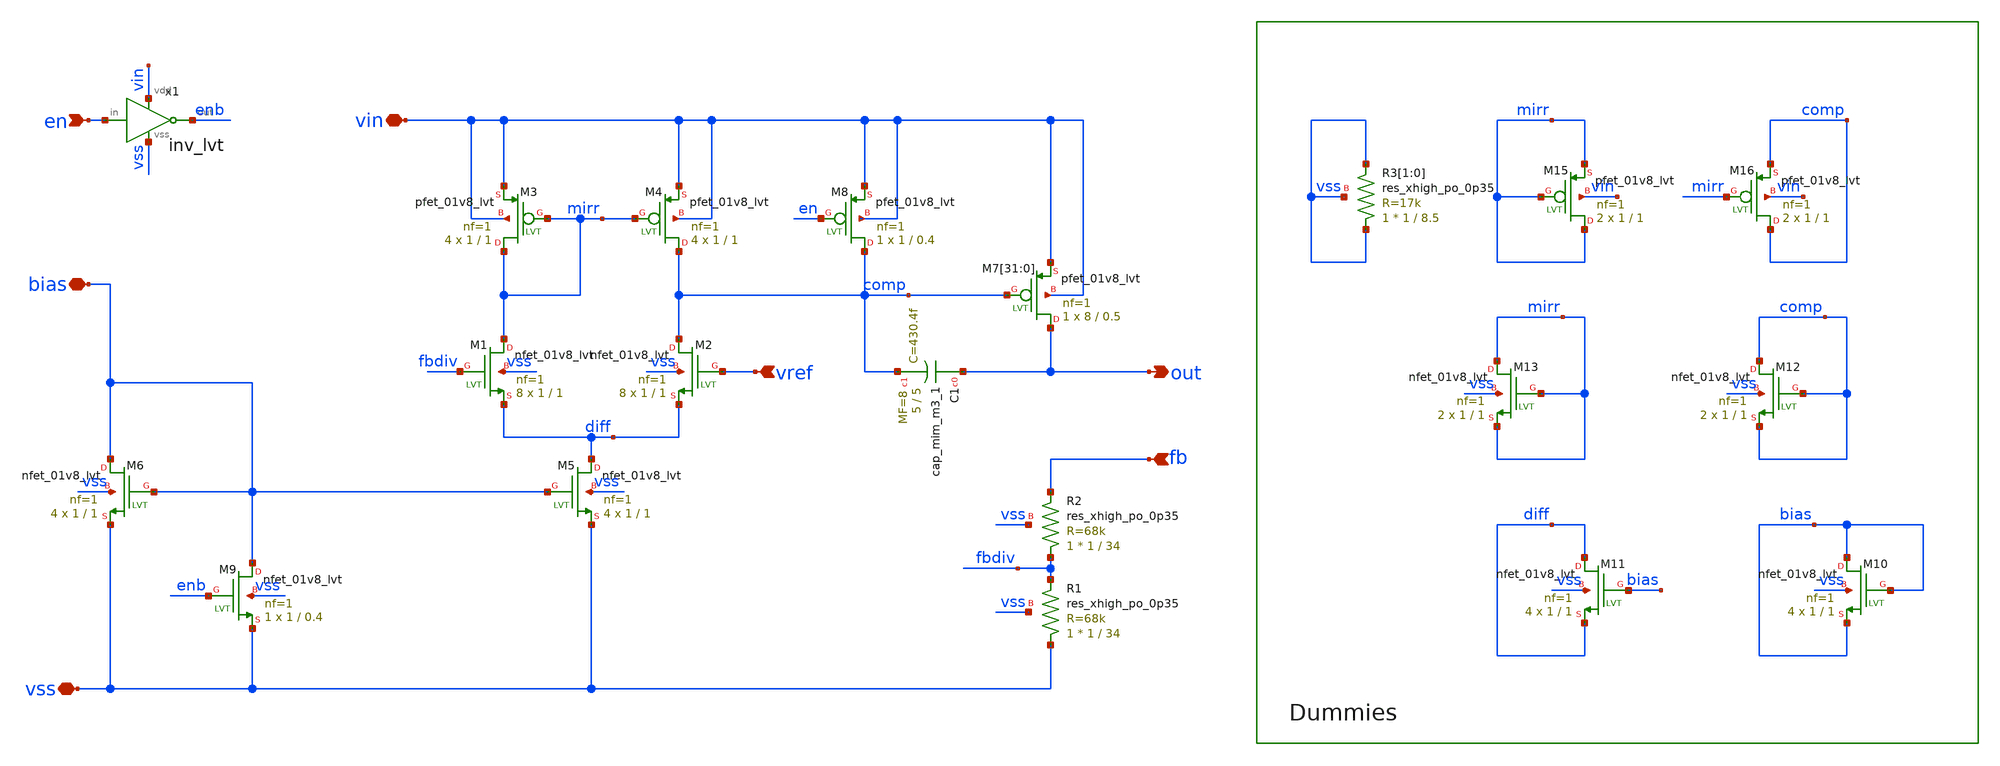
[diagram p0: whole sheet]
** sch_path: xschem/regulator/regulator.sch
**.subckt regulator vin vss vref out bias en fb
*.iopin vin
*.iopin vss
*.ipin vref
*.opin out
*.iopin bias
*.ipin en
*.ipin fb
XM2 comp vref diff vss sky130_fd_pr__nfet_01v8_lvt L=1 W=1 nf=1 ad='int((nf+1)/2) * W/nf * 0.29' as='int((nf+2)/2) * W/nf * 0.29'
+ pd='2*int((nf+1)/2) * (W/nf + 0.29)' ps='2*int((nf+2)/2) * (W/nf + 0.29)' nrd='0.29 / W' nrs='0.29 / W'
+ sa=0 sb=0 sd=0 mult=8 m=8
XM1 mirr fbdiv diff vss sky130_fd_pr__nfet_01v8_lvt L=1 W=1 nf=1 ad='int((nf+1)/2) * W/nf * 0.29' as='int((nf+2)/2) * W/nf * 0.29'
+ pd='2*int((nf+1)/2) * (W/nf + 0.29)' ps='2*int((nf+2)/2) * (W/nf + 0.29)' nrd='0.29 / W' nrs='0.29 / W'
+ sa=0 sb=0 sd=0 mult=8 m=8
XM5 diff bias vss vss sky130_fd_pr__nfet_01v8_lvt L=1 W=1 nf=1 ad='int((nf+1)/2) * W/nf * 0.29' as='int((nf+2)/2) * W/nf * 0.29'
+ pd='2*int((nf+1)/2) * (W/nf + 0.29)' ps='2*int((nf+2)/2) * (W/nf + 0.29)' nrd='0.29 / W' nrs='0.29 / W'
+ sa=0 sb=0 sd=0 mult=4 m=4
XM4 comp mirr vin vin sky130_fd_pr__pfet_01v8_lvt L=1 W=1 nf=1 ad='int((nf+1)/2) * W/nf * 0.29' as='int((nf+2)/2) * W/nf * 0.29'
+ pd='2*int((nf+1)/2) * (W/nf + 0.29)' ps='2*int((nf+2)/2) * (W/nf + 0.29)' nrd='0.29 / W' nrs='0.29 / W'
+ sa=0 sb=0 sd=0 mult=4 m=4
XM3 mirr mirr vin vin sky130_fd_pr__pfet_01v8_lvt L=1 W=1 nf=1 ad='int((nf+1)/2) * W/nf * 0.29' as='int((nf+2)/2) * W/nf * 0.29'
+ pd='2*int((nf+1)/2) * (W/nf + 0.29)' ps='2*int((nf+2)/2) * (W/nf + 0.29)' nrd='0.29 / W' nrs='0.29 / W'
+ sa=0 sb=0 sd=0 mult=4 m=4
XM6 bias bias vss vss sky130_fd_pr__nfet_01v8_lvt L=1 W=1 nf=1 ad='int((nf+1)/2) * W/nf * 0.29' as='int((nf+2)/2) * W/nf * 0.29'
+ pd='2*int((nf+1)/2) * (W/nf + 0.29)' ps='2*int((nf+2)/2) * (W/nf + 0.29)' nrd='0.29 / W' nrs='0.29 / W'
+ sa=0 sb=0 sd=0 mult=4 m=4
XM7[31] out comp vin vin sky130_fd_pr__pfet_01v8_lvt L=0.5 W=8 nf=1 ad='int((nf+1)/2) * W/nf * 0.29'
+ as='int((nf+2)/2) * W/nf * 0.29' pd='2*int((nf+1)/2) * (W/nf + 0.29)' ps='2*int((nf+2)/2) * (W/nf + 0.29)'
+ nrd='0.29 / W' nrs='0.29 / W' sa=0 sb=0 sd=0 mult=1 m=1
XM7[30] out comp vin vin sky130_fd_pr__pfet_01v8_lvt L=0.5 W=8 nf=1 ad='int((nf+1)/2) * W/nf * 0.29'
+ as='int((nf+2)/2) * W/nf * 0.29' pd='2*int((nf+1)/2) * (W/nf + 0.29)' ps='2*int((nf+2)/2) * (W/nf + 0.29)'
+ nrd='0.29 / W' nrs='0.29 / W' sa=0 sb=0 sd=0 mult=1 m=1
XM7[29] out comp vin vin sky130_fd_pr__pfet_01v8_lvt L=0.5 W=8 nf=1 ad='int((nf+1)/2) * W/nf * 0.29'
+ as='int((nf+2)/2) * W/nf * 0.29' pd='2*int((nf+1)/2) * (W/nf + 0.29)' ps='2*int((nf+2)/2) * (W/nf + 0.29)'
+ nrd='0.29 / W' nrs='0.29 / W' sa=0 sb=0 sd=0 mult=1 m=1
XM7[28] out comp vin vin sky130_fd_pr__pfet_01v8_lvt L=0.5 W=8 nf=1 ad='int((nf+1)/2) * W/nf * 0.29'
+ as='int((nf+2)/2) * W/nf * 0.29' pd='2*int((nf+1)/2) * (W/nf + 0.29)' ps='2*int((nf+2)/2) * (W/nf + 0.29)'
+ nrd='0.29 / W' nrs='0.29 / W' sa=0 sb=0 sd=0 mult=1 m=1
XM7[27] out comp vin vin sky130_fd_pr__pfet_01v8_lvt L=0.5 W=8 nf=1 ad='int((nf+1)/2) * W/nf * 0.29'
+ as='int((nf+2)/2) * W/nf * 0.29' pd='2*int((nf+1)/2) * (W/nf + 0.29)' ps='2*int((nf+2)/2) * (W/nf + 0.29)'
+ nrd='0.29 / W' nrs='0.29 / W' sa=0 sb=0 sd=0 mult=1 m=1
XM7[26] out comp vin vin sky130_fd_pr__pfet_01v8_lvt L=0.5 W=8 nf=1 ad='int((nf+1)/2) * W/nf * 0.29'
+ as='int((nf+2)/2) * W/nf * 0.29' pd='2*int((nf+1)/2) * (W/nf + 0.29)' ps='2*int((nf+2)/2) * (W/nf + 0.29)'
+ nrd='0.29 / W' nrs='0.29 / W' sa=0 sb=0 sd=0 mult=1 m=1
XM7[25] out comp vin vin sky130_fd_pr__pfet_01v8_lvt L=0.5 W=8 nf=1 ad='int((nf+1)/2) * W/nf * 0.29'
+ as='int((nf+2)/2) * W/nf * 0.29' pd='2*int((nf+1)/2) * (W/nf + 0.29)' ps='2*int((nf+2)/2) * (W/nf + 0.29)'
+ nrd='0.29 / W' nrs='0.29 / W' sa=0 sb=0 sd=0 mult=1 m=1
XM7[24] out comp vin vin sky130_fd_pr__pfet_01v8_lvt L=0.5 W=8 nf=1 ad='int((nf+1)/2) * W/nf * 0.29'
+ as='int((nf+2)/2) * W/nf * 0.29' pd='2*int((nf+1)/2) * (W/nf + 0.29)' ps='2*int((nf+2)/2) * (W/nf + 0.29)'
+ nrd='0.29 / W' nrs='0.29 / W' sa=0 sb=0 sd=0 mult=1 m=1
XM7[23] out comp vin vin sky130_fd_pr__pfet_01v8_lvt L=0.5 W=8 nf=1 ad='int((nf+1)/2) * W/nf * 0.29'
+ as='int((nf+2)/2) * W/nf * 0.29' pd='2*int((nf+1)/2) * (W/nf + 0.29)' ps='2*int((nf+2)/2) * (W/nf + 0.29)'
+ nrd='0.29 / W' nrs='0.29 / W' sa=0 sb=0 sd=0 mult=1 m=1
XM7[22] out comp vin vin sky130_fd_pr__pfet_01v8_lvt L=0.5 W=8 nf=1 ad='int((nf+1)/2) * W/nf * 0.29'
+ as='int((nf+2)/2) * W/nf * 0.29' pd='2*int((nf+1)/2) * (W/nf + 0.29)' ps='2*int((nf+2)/2) * (W/nf + 0.29)'
+ nrd='0.29 / W' nrs='0.29 / W' sa=0 sb=0 sd=0 mult=1 m=1
XM7[21] out comp vin vin sky130_fd_pr__pfet_01v8_lvt L=0.5 W=8 nf=1 ad='int((nf+1)/2) * W/nf * 0.29'
+ as='int((nf+2)/2) * W/nf * 0.29' pd='2*int((nf+1)/2) * (W/nf + 0.29)' ps='2*int((nf+2)/2) * (W/nf + 0.29)'
+ nrd='0.29 / W' nrs='0.29 / W' sa=0 sb=0 sd=0 mult=1 m=1
XM7[20] out comp vin vin sky130_fd_pr__pfet_01v8_lvt L=0.5 W=8 nf=1 ad='int((nf+1)/2) * W/nf * 0.29'
+ as='int((nf+2)/2) * W/nf * 0.29' pd='2*int((nf+1)/2) * (W/nf + 0.29)' ps='2*int((nf+2)/2) * (W/nf + 0.29)'
+ nrd='0.29 / W' nrs='0.29 / W' sa=0 sb=0 sd=0 mult=1 m=1
XM7[19] out comp vin vin sky130_fd_pr__pfet_01v8_lvt L=0.5 W=8 nf=1 ad='int((nf+1)/2) * W/nf * 0.29'
+ as='int((nf+2)/2) * W/nf * 0.29' pd='2*int((nf+1)/2) * (W/nf + 0.29)' ps='2*int((nf+2)/2) * (W/nf + 0.29)'
+ nrd='0.29 / W' nrs='0.29 / W' sa=0 sb=0 sd=0 mult=1 m=1
XM7[18] out comp vin vin sky130_fd_pr__pfet_01v8_lvt L=0.5 W=8 nf=1 ad='int((nf+1)/2) * W/nf * 0.29'
+ as='int((nf+2)/2) * W/nf * 0.29' pd='2*int((nf+1)/2) * (W/nf + 0.29)' ps='2*int((nf+2)/2) * (W/nf + 0.29)'
+ nrd='0.29 / W' nrs='0.29 / W' sa=0 sb=0 sd=0 mult=1 m=1
XM7[17] out comp vin vin sky130_fd_pr__pfet_01v8_lvt L=0.5 W=8 nf=1 ad='int((nf+1)/2) * W/nf * 0.29'
+ as='int((nf+2)/2) * W/nf * 0.29' pd='2*int((nf+1)/2) * (W/nf + 0.29)' ps='2*int((nf+2)/2) * (W/nf + 0.29)'
+ nrd='0.29 / W' nrs='0.29 / W' sa=0 sb=0 sd=0 mult=1 m=1
XM7[16] out comp vin vin sky130_fd_pr__pfet_01v8_lvt L=0.5 W=8 nf=1 ad='int((nf+1)/2) * W/nf * 0.29'
+ as='int((nf+2)/2) * W/nf * 0.29' pd='2*int((nf+1)/2) * (W/nf + 0.29)' ps='2*int((nf+2)/2) * (W/nf + 0.29)'
+ nrd='0.29 / W' nrs='0.29 / W' sa=0 sb=0 sd=0 mult=1 m=1
XM7[15] out comp vin vin sky130_fd_pr__pfet_01v8_lvt L=0.5 W=8 nf=1 ad='int((nf+1)/2) * W/nf * 0.29'
+ as='int((nf+2)/2) * W/nf * 0.29' pd='2*int((nf+1)/2) * (W/nf + 0.29)' ps='2*int((nf+2)/2) * (W/nf + 0.29)'
+ nrd='0.29 / W' nrs='0.29 / W' sa=0 sb=0 sd=0 mult=1 m=1
XM7[14] out comp vin vin sky130_fd_pr__pfet_01v8_lvt L=0.5 W=8 nf=1 ad='int((nf+1)/2) * W/nf * 0.29'
+ as='int((nf+2)/2) * W/nf * 0.29' pd='2*int((nf+1)/2) * (W/nf + 0.29)' ps='2*int((nf+2)/2) * (W/nf + 0.29)'
+ nrd='0.29 / W' nrs='0.29 / W' sa=0 sb=0 sd=0 mult=1 m=1
XM7[13] out comp vin vin sky130_fd_pr__pfet_01v8_lvt L=0.5 W=8 nf=1 ad='int((nf+1)/2) * W/nf * 0.29'
+ as='int((nf+2)/2) * W/nf * 0.29' pd='2*int((nf+1)/2) * (W/nf + 0.29)' ps='2*int((nf+2)/2) * (W/nf + 0.29)'
+ nrd='0.29 / W' nrs='0.29 / W' sa=0 sb=0 sd=0 mult=1 m=1
XM7[12] out comp vin vin sky130_fd_pr__pfet_01v8_lvt L=0.5 W=8 nf=1 ad='int((nf+1)/2) * W/nf * 0.29'
+ as='int((nf+2)/2) * W/nf * 0.29' pd='2*int((nf+1)/2) * (W/nf + 0.29)' ps='2*int((nf+2)/2) * (W/nf + 0.29)'
+ nrd='0.29 / W' nrs='0.29 / W' sa=0 sb=0 sd=0 mult=1 m=1
XM7[11] out comp vin vin sky130_fd_pr__pfet_01v8_lvt L=0.5 W=8 nf=1 ad='int((nf+1)/2) * W/nf * 0.29'
+ as='int((nf+2)/2) * W/nf * 0.29' pd='2*int((nf+1)/2) * (W/nf + 0.29)' ps='2*int((nf+2)/2) * (W/nf + 0.29)'
+ nrd='0.29 / W' nrs='0.29 / W' sa=0 sb=0 sd=0 mult=1 m=1
XM7[10] out comp vin vin sky130_fd_pr__pfet_01v8_lvt L=0.5 W=8 nf=1 ad='int((nf+1)/2) * W/nf * 0.29'
+ as='int((nf+2)/2) * W/nf * 0.29' pd='2*int((nf+1)/2) * (W/nf + 0.29)' ps='2*int((nf+2)/2) * (W/nf + 0.29)'
+ nrd='0.29 / W' nrs='0.29 / W' sa=0 sb=0 sd=0 mult=1 m=1
XM7[9] out comp vin vin sky130_fd_pr__pfet_01v8_lvt L=0.5 W=8 nf=1 ad='int((nf+1)/2) * W/nf * 0.29' as='int((nf+2)/2) * W/nf * 0.29'
+ pd='2*int((nf+1)/2) * (W/nf + 0.29)' ps='2*int((nf+2)/2) * (W/nf + 0.29)' nrd='0.29 / W' nrs='0.29 / W'
+ sa=0 sb=0 sd=0 mult=1 m=1
XM7[8] out comp vin vin sky130_fd_pr__pfet_01v8_lvt L=0.5 W=8 nf=1 ad='int((nf+1)/2) * W/nf * 0.29' as='int((nf+2)/2) * W/nf * 0.29'
+ pd='2*int((nf+1)/2) * (W/nf + 0.29)' ps='2*int((nf+2)/2) * (W/nf + 0.29)' nrd='0.29 / W' nrs='0.29 / W'
+ sa=0 sb=0 sd=0 mult=1 m=1
XM7[7] out comp vin vin sky130_fd_pr__pfet_01v8_lvt L=0.5 W=8 nf=1 ad='int((nf+1)/2) * W/nf * 0.29' as='int((nf+2)/2) * W/nf * 0.29'
+ pd='2*int((nf+1)/2) * (W/nf + 0.29)' ps='2*int((nf+2)/2) * (W/nf + 0.29)' nrd='0.29 / W' nrs='0.29 / W'
+ sa=0 sb=0 sd=0 mult=1 m=1
XM7[6] out comp vin vin sky130_fd_pr__pfet_01v8_lvt L=0.5 W=8 nf=1 ad='int((nf+1)/2) * W/nf * 0.29' as='int((nf+2)/2) * W/nf * 0.29'
+ pd='2*int((nf+1)/2) * (W/nf + 0.29)' ps='2*int((nf+2)/2) * (W/nf + 0.29)' nrd='0.29 / W' nrs='0.29 / W'
+ sa=0 sb=0 sd=0 mult=1 m=1
XM7[5] out comp vin vin sky130_fd_pr__pfet_01v8_lvt L=0.5 W=8 nf=1 ad='int((nf+1)/2) * W/nf * 0.29' as='int((nf+2)/2) * W/nf * 0.29'
+ pd='2*int((nf+1)/2) * (W/nf + 0.29)' ps='2*int((nf+2)/2) * (W/nf + 0.29)' nrd='0.29 / W' nrs='0.29 / W'
+ sa=0 sb=0 sd=0 mult=1 m=1
XM7[4] out comp vin vin sky130_fd_pr__pfet_01v8_lvt L=0.5 W=8 nf=1 ad='int((nf+1)/2) * W/nf * 0.29' as='int((nf+2)/2) * W/nf * 0.29'
+ pd='2*int((nf+1)/2) * (W/nf + 0.29)' ps='2*int((nf+2)/2) * (W/nf + 0.29)' nrd='0.29 / W' nrs='0.29 / W'
+ sa=0 sb=0 sd=0 mult=1 m=1
XM7[3] out comp vin vin sky130_fd_pr__pfet_01v8_lvt L=0.5 W=8 nf=1 ad='int((nf+1)/2) * W/nf * 0.29' as='int((nf+2)/2) * W/nf * 0.29'
+ pd='2*int((nf+1)/2) * (W/nf + 0.29)' ps='2*int((nf+2)/2) * (W/nf + 0.29)' nrd='0.29 / W' nrs='0.29 / W'
+ sa=0 sb=0 sd=0 mult=1 m=1
XM7[2] out comp vin vin sky130_fd_pr__pfet_01v8_lvt L=0.5 W=8 nf=1 ad='int((nf+1)/2) * W/nf * 0.29' as='int((nf+2)/2) * W/nf * 0.29'
+ pd='2*int((nf+1)/2) * (W/nf + 0.29)' ps='2*int((nf+2)/2) * (W/nf + 0.29)' nrd='0.29 / W' nrs='0.29 / W'
+ sa=0 sb=0 sd=0 mult=1 m=1
XM7[1] out comp vin vin sky130_fd_pr__pfet_01v8_lvt L=0.5 W=8 nf=1 ad='int((nf+1)/2) * W/nf * 0.29' as='int((nf+2)/2) * W/nf * 0.29'
+ pd='2*int((nf+1)/2) * (W/nf + 0.29)' ps='2*int((nf+2)/2) * (W/nf + 0.29)' nrd='0.29 / W' nrs='0.29 / W'
+ sa=0 sb=0 sd=0 mult=1 m=1
XM7[0] out comp vin vin sky130_fd_pr__pfet_01v8_lvt L=0.5 W=8 nf=1 ad='int((nf+1)/2) * W/nf * 0.29' as='int((nf+2)/2) * W/nf * 0.29'
+ pd='2*int((nf+1)/2) * (W/nf + 0.29)' ps='2*int((nf+2)/2) * (W/nf + 0.29)' nrd='0.29 / W' nrs='0.29 / W'
+ sa=0 sb=0 sd=0 mult=1 m=1
XC1 out comp sky130_fd_pr__cap_mim_m3_1 W=5 L=5 MF=8 m=8
XM9 bias enb vss vss sky130_fd_pr__nfet_01v8_lvt L=0.4 W=1 nf=1 ad='int((nf+1)/2) * W/nf * 0.29' as='int((nf+2)/2) * W/nf * 0.29'
+ pd='2*int((nf+1)/2) * (W/nf + 0.29)' ps='2*int((nf+2)/2) * (W/nf + 0.29)' nrd='0.29 / W' nrs='0.29 / W'
+ sa=0 sb=0 sd=0 mult=1 m=1
x1 vin en enb vss inv_lvt
XM8 comp en vin vin sky130_fd_pr__pfet_01v8_lvt L=0.4 W=1 nf=1 ad='int((nf+1)/2) * W/nf * 0.29' as='int((nf+2)/2) * W/nf * 0.29'
+ pd='2*int((nf+1)/2) * (W/nf + 0.29)' ps='2*int((nf+2)/2) * (W/nf + 0.29)' nrd='0.29 / W' nrs='0.29 / W'
+ sa=0 sb=0 sd=0 mult=1 m=1
XM10 bias bias bias vss sky130_fd_pr__nfet_01v8_lvt L=1 W=1 nf=1 ad='int((nf+1)/2) * W/nf * 0.29' as='int((nf+2)/2) * W/nf * 0.29'
+ pd='2*int((nf+1)/2) * (W/nf + 0.29)' ps='2*int((nf+2)/2) * (W/nf + 0.29)' nrd='0.29 / W' nrs='0.29 / W'
+ sa=0 sb=0 sd=0 mult=4 m=4
XM11 diff bias diff vss sky130_fd_pr__nfet_01v8_lvt L=1 W=1 nf=1 ad='int((nf+1)/2) * W/nf * 0.29' as='int((nf+2)/2) * W/nf * 0.29'
+ pd='2*int((nf+1)/2) * (W/nf + 0.29)' ps='2*int((nf+2)/2) * (W/nf + 0.29)' nrd='0.29 / W' nrs='0.29 / W'
+ sa=0 sb=0 sd=0 mult=4 m=4
XM12 comp comp comp vss sky130_fd_pr__nfet_01v8_lvt L=1 W=1 nf=1 ad='int((nf+1)/2) * W/nf * 0.29' as='int((nf+2)/2) * W/nf * 0.29'
+ pd='2*int((nf+1)/2) * (W/nf + 0.29)' ps='2*int((nf+2)/2) * (W/nf + 0.29)' nrd='0.29 / W' nrs='0.29 / W'
+ sa=0 sb=0 sd=0 mult=2 m=2
XM13 mirr mirr mirr vss sky130_fd_pr__nfet_01v8_lvt L=1 W=1 nf=1 ad='int((nf+1)/2) * W/nf * 0.29' as='int((nf+2)/2) * W/nf * 0.29'
+ pd='2*int((nf+1)/2) * (W/nf + 0.29)' ps='2*int((nf+2)/2) * (W/nf + 0.29)' nrd='0.29 / W' nrs='0.29 / W'
+ sa=0 sb=0 sd=0 mult=2 m=2
XM15 mirr mirr mirr vin sky130_fd_pr__pfet_01v8_lvt L=1 W=1 nf=1 ad='int((nf+1)/2) * W/nf * 0.29' as='int((nf+2)/2) * W/nf * 0.29'
+ pd='2*int((nf+1)/2) * (W/nf + 0.29)' ps='2*int((nf+2)/2) * (W/nf + 0.29)' nrd='0.29 / W' nrs='0.29 / W'
+ sa=0 sb=0 sd=0 mult=2 m=2
XM16 comp mirr comp vin sky130_fd_pr__pfet_01v8_lvt L=1 W=1 nf=1 ad='int((nf+1)/2) * W/nf * 0.29' as='int((nf+2)/2) * W/nf * 0.29'
+ pd='2*int((nf+1)/2) * (W/nf + 0.29)' ps='2*int((nf+2)/2) * (W/nf + 0.29)' nrd='0.29 / W' nrs='0.29 / W'
+ sa=0 sb=0 sd=0 mult=2 m=2
XR2 fbdiv fb vss sky130_fd_pr__res_xhigh_po_0p35 W=1 L=34 mult=1 m=1
XR1 vss fbdiv vss sky130_fd_pr__res_xhigh_po_0p35 W=1 L=34 mult=1 m=1
XR3[1] vss vss vss sky130_fd_pr__res_xhigh_po_0p35 W=1 L=8.5 mult=1 m=1
XR3[0] vss vss vss sky130_fd_pr__res_xhigh_po_0p35 W=1 L=8.5 mult=1 m=1
**.ends

* expanding   symbol:  logic/inv_lvt.sym # of pins=4
** sym_path: logic/inv_lvt.sym
** sch_path: logic/inv_lvt.sch
.subckt inv_lvt vdd in out vss
*.iopin vdd
*.iopin vss
*.ipin in
*.opin out
XM1 out in vss vss sky130_fd_pr__nfet_01v8_lvt L=0.4 W=1 nf=1 ad='int((nf+1)/2) * W/nf * 0.29' as='int((nf+2)/2) * W/nf * 0.29'
+ pd='2*int((nf+1)/2) * (W/nf + 0.29)' ps='2*int((nf+2)/2) * (W/nf + 0.29)' nrd='0.29 / W' nrs='0.29 / W'
+ sa=0 sb=0 sd=0 mult=1 m=1
XM2 out in vdd vdd sky130_fd_pr__pfet_01v8_lvt L=0.4 W=1 nf=1 ad='int((nf+1)/2) * W/nf * 0.29' as='int((nf+2)/2) * W/nf * 0.29'
+ pd='2*int((nf+1)/2) * (W/nf + 0.29)' ps='2*int((nf+2)/2) * (W/nf + 0.29)' nrd='0.29 / W' nrs='0.29 / W'
+ sa=0 sb=0 sd=0 mult=1 m=1
.ends

.end
